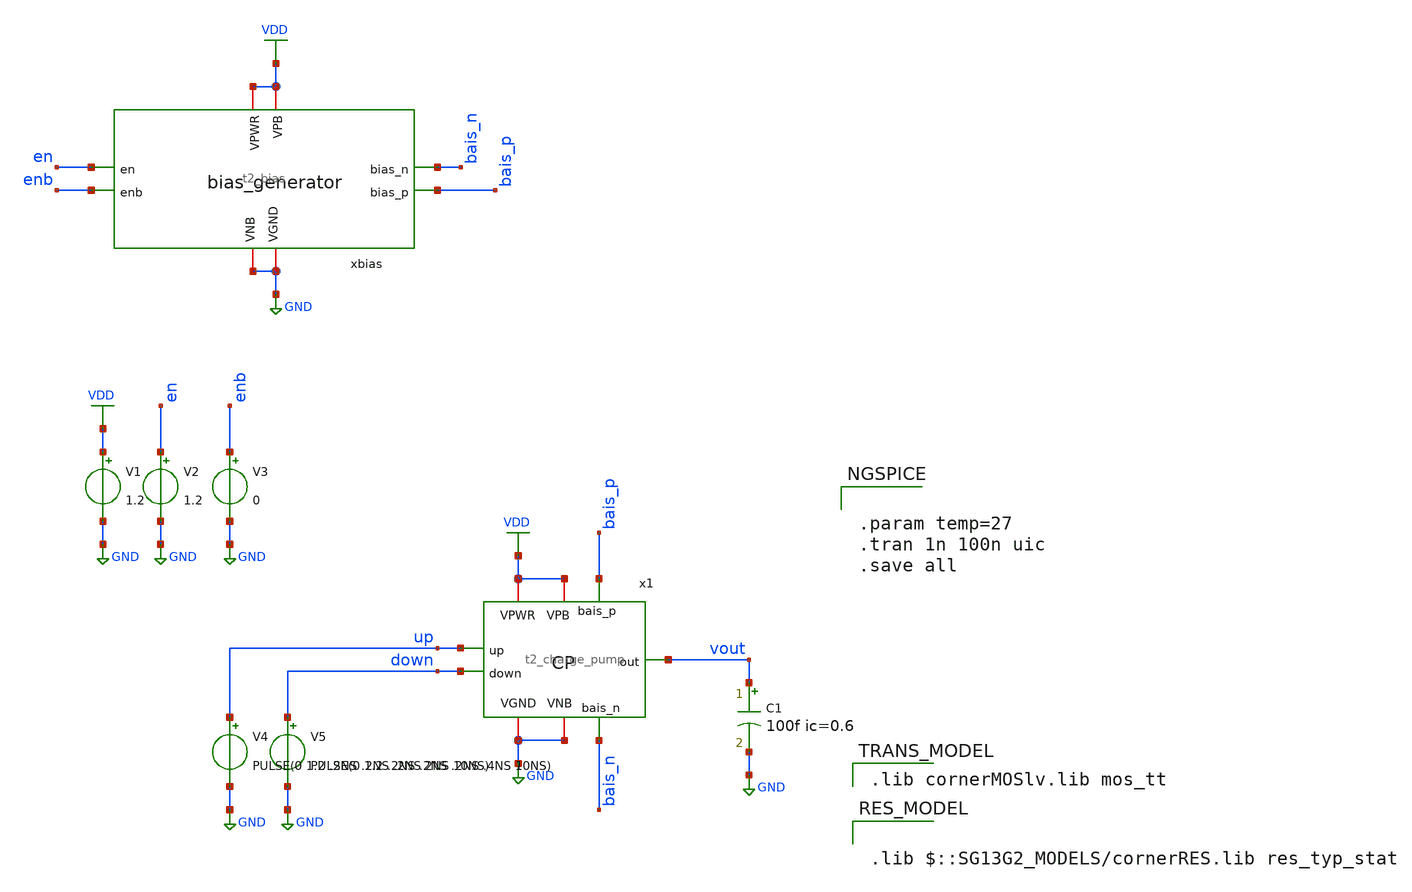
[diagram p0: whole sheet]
** sch_path: Team 2 Design/design_data/xschem/t2_charge_pump_tb.sch
**.subckt t2_charge_pump_tb
V1 VDD GND 1.2
V2 en GND 1.2
V3 enb GND 0
V4 up GND PULSE(0 1.2 .2NS .2NS .2NS 2NS 10NS)
V5 down GND PULSE(0 1.2 .2NS .2NS .2NS .4NS 10NS)
C1 vout GND 100f ic=0.6 m=1
x1 VDD VDD GND GND vout up down bais_p bais_n t2_charge_pump
x2 VDD VDD GND GND en bais_n bais_p enb t2_bias
**** begin user architecture code


.param temp=27
.tran 1n 100n uic
.save all


 .lib cornerMOSlv.lib mos_tt


.lib $::SG13G2_MODELS/cornerRES.lib res_typ_stat

**** end user architecture code
**.ends

* expanding   symbol:  t2_charge_pump.sym # of pins=9
** sym_path: Team 2 Design/design_data/xschem/t2_charge_pump.sym
** sch_path: Team 2 Design/design_data/xschem/t2_charge_pump.sch
.subckt t2_charge_pump VPWR VPB VGND VNB out up down bais_p bais_n
*.iopin VPWR
*.ipin up
*.opin out
*.iopin VPB
*.iopin VGND
*.iopin VNB
*.ipin down
*.ipin bais_p
*.ipin bais_n
XM1 i_down bais_n VGND VNB sg13_lv_nmos w=0.5u l=0.13u ng=1 m=1 mm_ok=1
XM2 out down i_down VNB sg13_lv_nmos w=0.15u l=0.13u ng=1 m=1 mm_ok=1
XM3 i_up bais_p VPWR VPB sg13_lv_pmos w=0.15u l=0.13u ng=1 m=1 mm_ok=1
XM4 out net1 i_up VPB sg13_lv_pmos w=0.3u l=0.13u ng=1 m=1 mm_ok=1
x1 VPWR up net1 VGND t2_inverter
.ends


* expanding   symbol:  t2_bias.sym # of pins=8
** sym_path: Team Designs/Team 2 Design/design_data/xschem/t2_bias.sym
** sch_path: Team Designs/Team 2 Design/design_data/xschem/t2_bias.sch
.subckt t2_bias VPWR VPB VGND VNB en bias_n bias_p enb
*.iopin VPWR
*.iopin VPB
*.iopin VGND
*.iopin VNB
*.ipin en
*.ipin enb
*.opin bias_n
*.opin bias_p
XM9 net1 en VPWR VPB sg13_lv_pmos w=0.5u l=0.15u ng=1 m=1 mm_ok=1
XM10 bias_p bias_p VPWR VPB sg13_lv_pmos w=0.2u l=1.0u ng=1 m=5 mm_ok=1
XM1 dio_mid dio_mid VPWR VPB sg13_lv_pmos w=0.5u l=0.15u ng=1 m=1 mm_ok=1
XM2 net1 net1 dio_mid VPB sg13_lv_pmos w=0.5u l=0.15u ng=1 m=1 mm_ok=1
XM3 bias_p en VPWR VPB sg13_lv_pmos w=0.5u l=0.15u ng=1 m=1 mm_ok=1
XM4 bias_n bias_p res_bot VPB sg13_lv_pmos w=0.2u l=1.0u ng=1 m=5 mm_ok=1
XM11 kick_sw en VGND VNB sg13_lv_nmos w=0.5u l=0.15u ng=1 m=1 mm_ok=1
XM12 bias_p net1 kick_sw VNB sg13_lv_nmos w=0.5u l=0.15u ng=1 m=1 mm_ok=1
XM5 net1 bias_n VGND VNB sg13_lv_nmos w=0.2u l=1.0u ng=1 m=5 mm_ok=1
XM6 bias_p bias_n VGND VNB sg13_lv_nmos w=0.2u l=1.0u ng=1 m=5 mm_ok=1
XM7 bias_n enb VGND VNB sg13_lv_nmos w=0.5u l=0.15u ng=1 m=1 mm_ok=1
XM8 bias_n bias_n VGND VNB sg13_lv_nmos w=0.2u l=1.0u ng=1 m=5 mm_ok=1
XR1 VPWR res_bot sub! rhigh w=0.5e-6 l=0.5e-6 m=1 b=0 mm_ok=1
.ends


* expanding   symbol:  t2_inverter.sym # of pins=4
** sym_path: Team 2 Design/design_data/xschem/t2_inverter.sym
** sch_path: Team 2 Design/design_data/xschem/t2_inverter.sch
.subckt t2_inverter VP A Y VN
*.iopin VP
*.iopin VN
*.ipin A
*.opin Y
XM2 Y A VP VP sg13_lv_pmos w=0.3u l=0.13u ng=1 m=1 mm_ok=1
XM1 Y A VN VN sg13_lv_nmos w=0.15u l=0.13u ng=1 m=1 mm_ok=1
.ends

.GLOBAL GND
.GLOBAL VDD
.end
